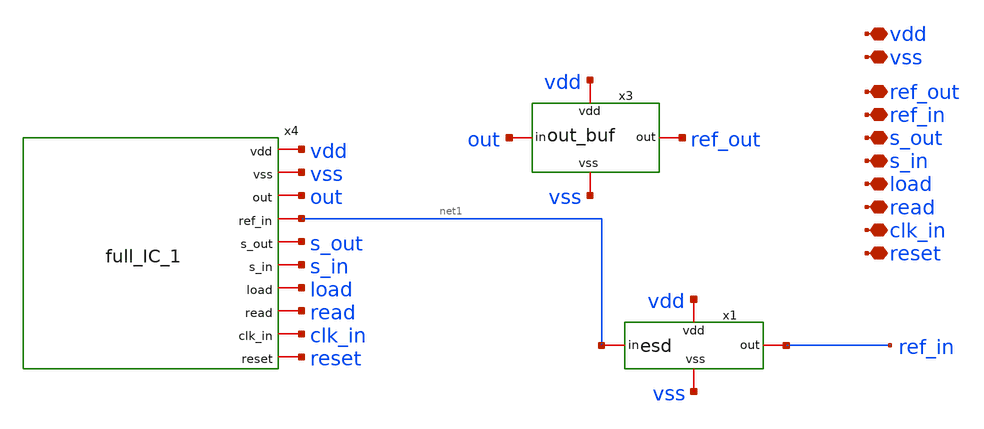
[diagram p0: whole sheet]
** sch_path: xschem/complete_wrapper.sch
**.subckt complete_wrapper vss vdd s_out s_in reset ref_out ref_in read load clk_in
*.iopin vss
*.iopin vdd
*.iopin s_out
*.iopin s_in
*.iopin reset
*.iopin ref_out
*.iopin ref_in
*.iopin read
*.iopin load
*.iopin clk_in
x3 vdd ref_out out vss out_buf
x4 vdd vss net1 s_out s_in load read clk_in reset out full_IC_1
x1 net1 vdd vss ref_in esd
**.ends
.end
